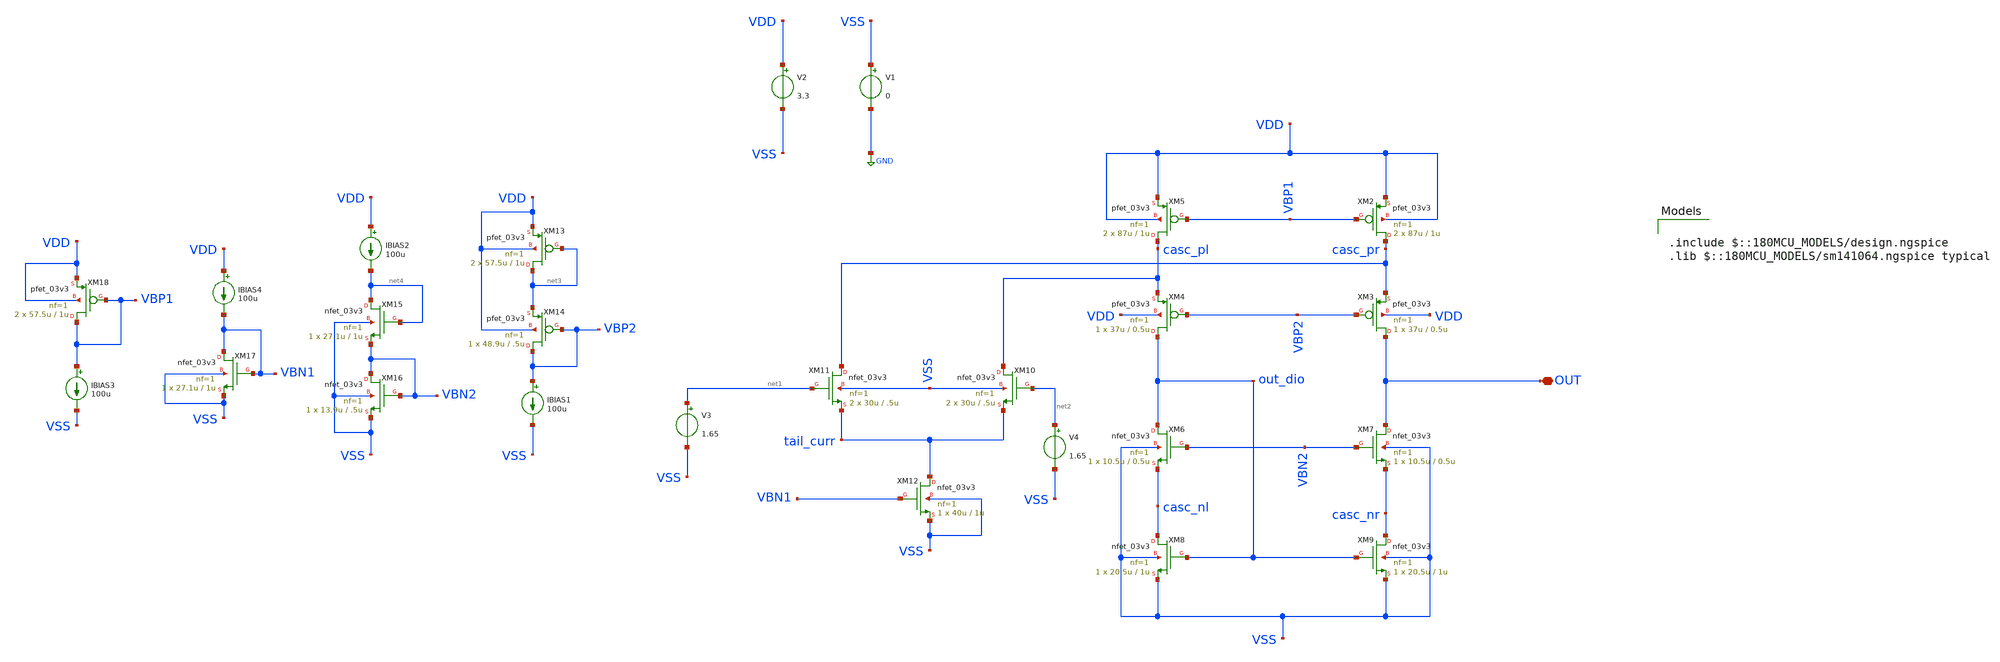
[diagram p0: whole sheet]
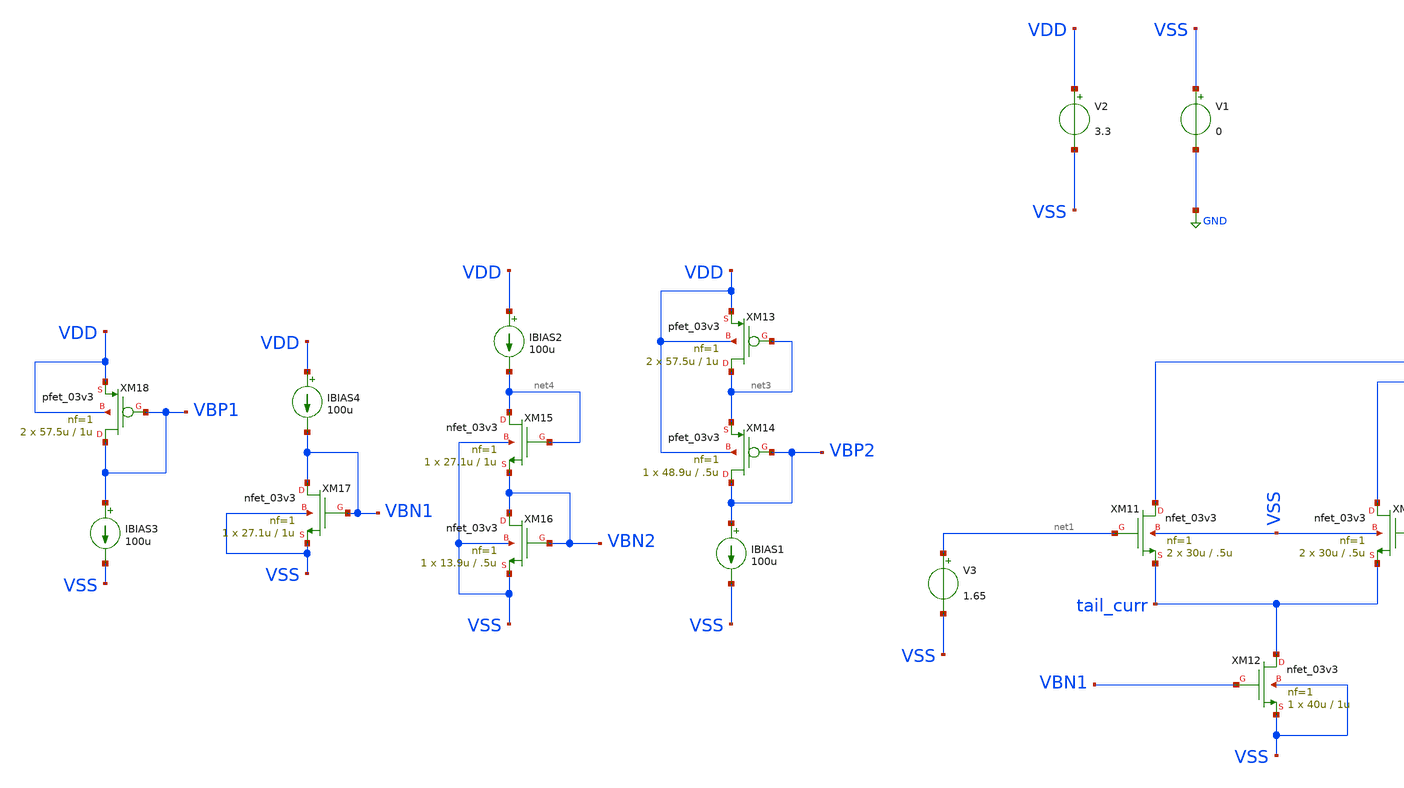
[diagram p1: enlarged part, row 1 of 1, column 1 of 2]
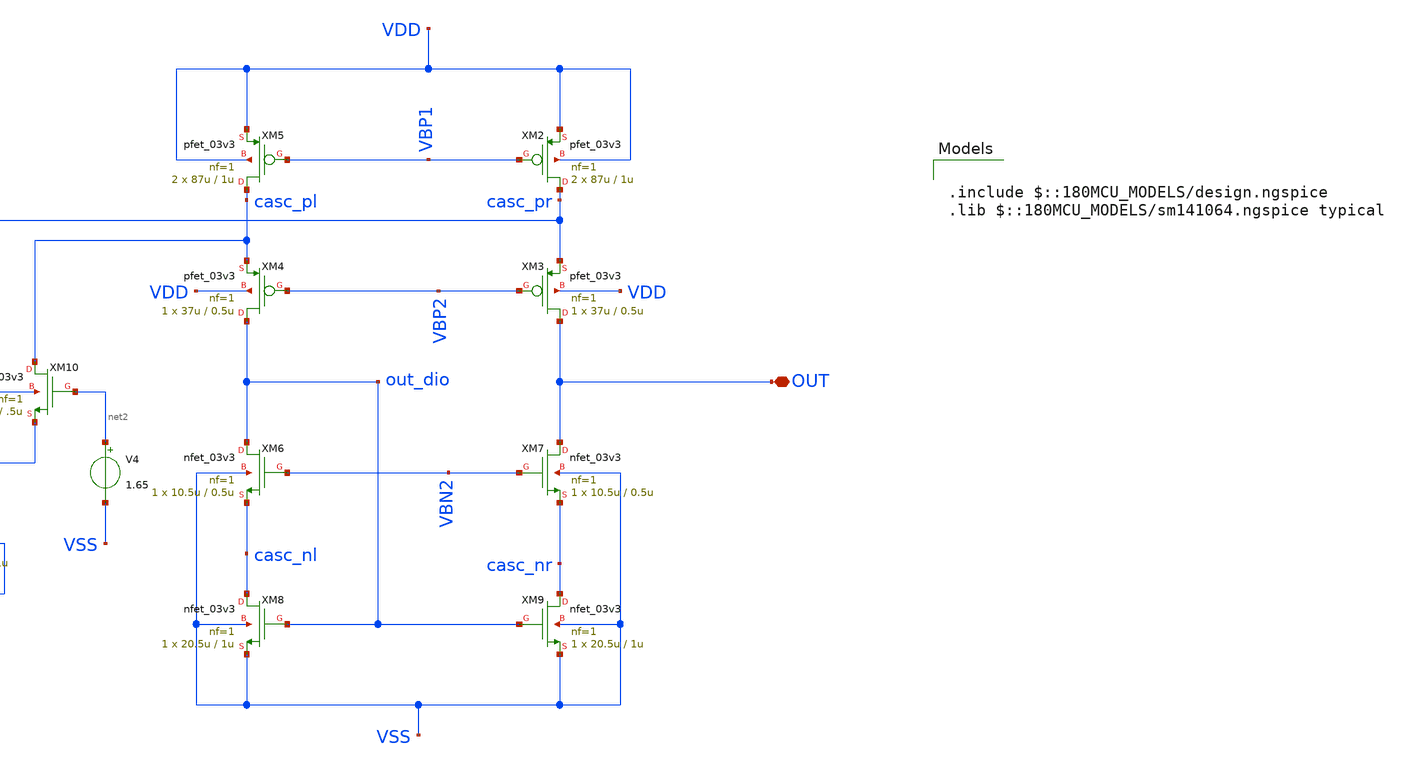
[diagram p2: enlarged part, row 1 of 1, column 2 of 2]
** sch_path: designs/libs/core_amps/ota_folded_cascode/etj_folded_new.sch
**.subckt etj_folded_new OUT
*.iopin OUT
XM2 casc_pr VBP1 VDD VDD pfet_03v3 L=1u W=87u nf=1 ad='int((nf+1)/2) * W/nf * 0.18u' as='int((nf+2)/2) * W/nf * 0.18u'
+ pd='2*int((nf+1)/2) * (W/nf + 0.18u)' ps='2*int((nf+2)/2) * (W/nf + 0.18u)' nrd='0.18u / W' nrs='0.18u / W'
+ sa=0 sb=0 sd=0 m=2
XM3 OUT VBP2 casc_pr VDD pfet_03v3 L=0.5u W=37u nf=1 ad='int((nf+1)/2) * W/nf * 0.18u' as='int((nf+2)/2) * W/nf * 0.18u'
+ pd='2*int((nf+1)/2) * (W/nf + 0.18u)' ps='2*int((nf+2)/2) * (W/nf + 0.18u)' nrd='0.18u / W' nrs='0.18u / W'
+ sa=0 sb=0 sd=0 m=1
XM4 out_dio VBP2 casc_pl VDD pfet_03v3 L=0.5u W=37u nf=1 ad='int((nf+1)/2) * W/nf * 0.18u' as='int((nf+2)/2) * W/nf * 0.18u'
+ pd='2*int((nf+1)/2) * (W/nf + 0.18u)' ps='2*int((nf+2)/2) * (W/nf + 0.18u)' nrd='0.18u / W' nrs='0.18u / W'
+ sa=0 sb=0 sd=0 m=1
XM5 casc_pl VBP1 VDD VDD pfet_03v3 L=1u W=87u nf=1 ad='int((nf+1)/2) * W/nf * 0.18u' as='int((nf+2)/2) * W/nf * 0.18u'
+ pd='2*int((nf+1)/2) * (W/nf + 0.18u)' ps='2*int((nf+2)/2) * (W/nf + 0.18u)' nrd='0.18u / W' nrs='0.18u / W'
+ sa=0 sb=0 sd=0 m=2
XM6 out_dio VBN2 casc_nl VSS nfet_03v3 L=0.5u W=10.5u nf=1 ad='int((nf+1)/2) * W/nf * 0.18u' as='int((nf+2)/2) * W/nf * 0.18u'
+ pd='2*int((nf+1)/2) * (W/nf + 0.18u)' ps='2*int((nf+2)/2) * (W/nf + 0.18u)' nrd='0.18u / W' nrs='0.18u / W'
+ sa=0 sb=0 sd=0 m=1
XM7 OUT VBN2 casc_nr VSS nfet_03v3 L=0.5u W=10.5u nf=1 ad='int((nf+1)/2) * W/nf * 0.18u' as='int((nf+2)/2) * W/nf * 0.18u'
+ pd='2*int((nf+1)/2) * (W/nf + 0.18u)' ps='2*int((nf+2)/2) * (W/nf + 0.18u)' nrd='0.18u / W' nrs='0.18u / W'
+ sa=0 sb=0 sd=0 m=1
XM8 casc_nl out_dio VSS VSS nfet_03v3 L=1u W=20.5u nf=1 ad='int((nf+1)/2) * W/nf * 0.18u' as='int((nf+2)/2) * W/nf * 0.18u'
+ pd='2*int((nf+1)/2) * (W/nf + 0.18u)' ps='2*int((nf+2)/2) * (W/nf + 0.18u)' nrd='0.18u / W' nrs='0.18u / W'
+ sa=0 sb=0 sd=0 m=1
XM9 casc_nr out_dio VSS VSS nfet_03v3 L=1u W=20.5u nf=1 ad='int((nf+1)/2) * W/nf * 0.18u' as='int((nf+2)/2) * W/nf * 0.18u'
+ pd='2*int((nf+1)/2) * (W/nf + 0.18u)' ps='2*int((nf+2)/2) * (W/nf + 0.18u)' nrd='0.18u / W' nrs='0.18u / W'
+ sa=0 sb=0 sd=0 m=1
XM10 casc_pl net2 tail_curr VSS nfet_03v3 L=.5u W=30u nf=1 ad='int((nf+1)/2) * W/nf * 0.18u' as='int((nf+2)/2) * W/nf * 0.18u'
+ pd='2*int((nf+1)/2) * (W/nf + 0.18u)' ps='2*int((nf+2)/2) * (W/nf + 0.18u)' nrd='0.18u / W' nrs='0.18u / W'
+ sa=0 sb=0 sd=0 m=2
XM12 tail_curr VBN1 VSS VSS nfet_03v3 L=1u W=40u nf=1 ad='int((nf+1)/2) * W/nf * 0.18u' as='int((nf+2)/2) * W/nf * 0.18u'
+ pd='2*int((nf+1)/2) * (W/nf + 0.18u)' ps='2*int((nf+2)/2) * (W/nf + 0.18u)' nrd='0.18u / W' nrs='0.18u / W'
+ sa=0 sb=0 sd=0 m=1
XM11 casc_pr net1 tail_curr VSS nfet_03v3 L=.5u W=30u nf=1 ad='int((nf+1)/2) * W/nf * 0.18u' as='int((nf+2)/2) * W/nf * 0.18u'
+ pd='2*int((nf+1)/2) * (W/nf + 0.18u)' ps='2*int((nf+2)/2) * (W/nf + 0.18u)' nrd='0.18u / W' nrs='0.18u / W'
+ sa=0 sb=0 sd=0 m=2
V2 VDD VSS 3.3
V1 VSS GND 0
V3 net1 VSS 1.65
V4 net2 VSS 1.65
XM13 net3 net3 VDD VDD pfet_03v3 L=1u W=57.5u nf=1 ad='int((nf+1)/2) * W/nf * 0.18u' as='int((nf+2)/2) * W/nf * 0.18u'
+ pd='2*int((nf+1)/2) * (W/nf + 0.18u)' ps='2*int((nf+2)/2) * (W/nf + 0.18u)' nrd='0.18u / W' nrs='0.18u / W'
+ sa=0 sb=0 sd=0 m=2
IBIAS1 VBP2 VSS 100u
XM14 VBP2 VBP2 net3 VDD pfet_03v3 L=.5u W=48.9u nf=1 ad='int((nf+1)/2) * W/nf * 0.18u' as='int((nf+2)/2) * W/nf * 0.18u'
+ pd='2*int((nf+1)/2) * (W/nf + 0.18u)' ps='2*int((nf+2)/2) * (W/nf + 0.18u)' nrd='0.18u / W' nrs='0.18u / W'
+ sa=0 sb=0 sd=0 m=1
IBIAS2 VDD net4 100u
XM15 net4 net4 VBN2 VSS nfet_03v3 L=1u W=27.1u nf=1 ad='int((nf+1)/2) * W/nf * 0.18u' as='int((nf+2)/2) * W/nf * 0.18u'
+ pd='2*int((nf+1)/2) * (W/nf + 0.18u)' ps='2*int((nf+2)/2) * (W/nf + 0.18u)' nrd='0.18u / W' nrs='0.18u / W'
+ sa=0 sb=0 sd=0 m=1
XM16 VBN2 VBN2 VSS VSS nfet_03v3 L=.5u W=13.9u nf=1 ad='int((nf+1)/2) * W/nf * 0.18u' as='int((nf+2)/2) * W/nf * 0.18u'
+ pd='2*int((nf+1)/2) * (W/nf + 0.18u)' ps='2*int((nf+2)/2) * (W/nf + 0.18u)' nrd='0.18u / W' nrs='0.18u / W'
+ sa=0 sb=0 sd=0 m=1
XM17 VBN1 VBN1 VSS VSS nfet_03v3 L=1u W=27.1u nf=1 ad='int((nf+1)/2) * W/nf * 0.18u' as='int((nf+2)/2) * W/nf * 0.18u'
+ pd='2*int((nf+1)/2) * (W/nf + 0.18u)' ps='2*int((nf+2)/2) * (W/nf + 0.18u)' nrd='0.18u / W' nrs='0.18u / W'
+ sa=0 sb=0 sd=0 m=1
XM18 VBP1 VBP1 VDD VDD pfet_03v3 L=1u W=57.5u nf=1 ad='int((nf+1)/2) * W/nf * 0.18u' as='int((nf+2)/2) * W/nf * 0.18u'
+ pd='2*int((nf+1)/2) * (W/nf + 0.18u)' ps='2*int((nf+2)/2) * (W/nf + 0.18u)' nrd='0.18u / W' nrs='0.18u / W'
+ sa=0 sb=0 sd=0 m=2
IBIAS3 VBP1 VSS 100u
IBIAS4 VDD VBN1 100u
**** begin user architecture code

.include $::180MCU_MODELS/design.ngspice
.lib $::180MCU_MODELS/sm141064.ngspice typical



.control
op
let gmid_xm17 = @m.xm17.m0[gm]/@m.xm17.m0[id]
let gmid_xm16 = @m.xm16.m0[gm]/@m.xm16.m0[id]
let gmid_xm15 = @m.xm15.m0[gm]/@m.xm15.m0[id]
let gmid_xm11 = @m.xm11.m0[gm]/@m.xm11.m0[id]
let gmid_xm12 = @m.xm12.m0[gm]/@m.xm12.m0[id]
let gmid_xm10 = @m.xm10.m0[gm]/@m.xm10.m0[id]
let gmid_xm9  = @m.xm9.m0[gm]/@m.xm9.m0[id]
let gmid_xm8  = @m.xm8.m0[gm]/@m.xm8.m0[id]
let gmid_xm7  = @m.xm7.m0[gm]/@m.xm7.m0[id]
let gmid_xm6  = @m.xm6.m0[gm]/@m.xm6.m0[id]
let gmid_xm18 = @m.xm18.m0[gm]/@m.xm18.m0[id]
let gmid_xm14 = @m.xm14.m0[gm]/@m.xm14.m0[id]
let gmid_xm13 = @m.xm13.m0[gm]/@m.xm13.m0[id]
let gmid_xm5  = @m.xm5.m0[gm]/@m.xm5.m0[id]
let gmid_xm4  = @m.xm4.m0[gm]/@m.xm4.m0[id]
let gmid_xm3  = @m.xm3.m0[gm]/@m.xm3.m0[id]
let gmid_xm2  = @m.xm2.m0[gm]/@m.xm2.m0[id]
print gmid_xm17 gmid_xm16 gmid_xm15 gmid_xm11 gmid_xm12
print gmid_xm10 gmid_xm9 gmid_xm8 gmid_xm7 gmid_xm6
print gmid_xm18 gmid_xm14 gmid_xm13 gmid_xm5 gmid_xm4
print gmid_xm3 gmid_xm2

.endc


**** end user architecture code
**.ends
.GLOBAL GND
.end
